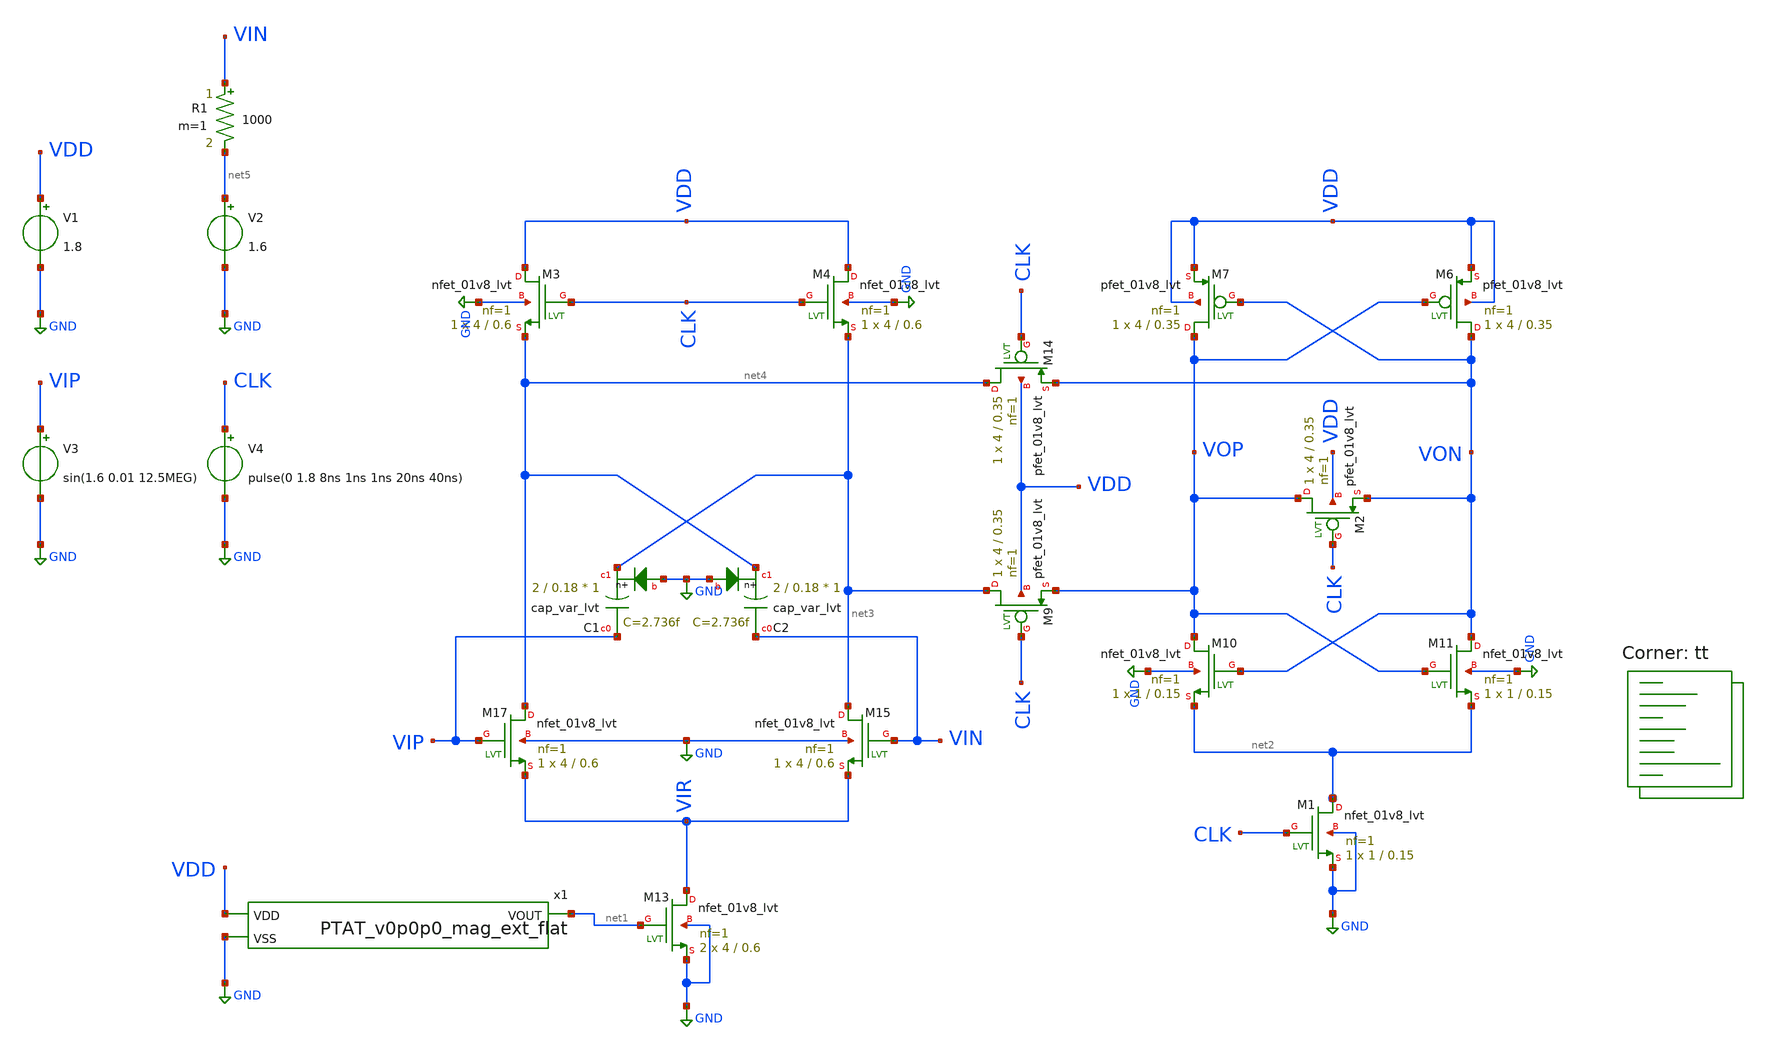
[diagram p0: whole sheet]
** sch_path: PTAT/xschem/class_AB_PTAT_ext.sch
**.subckt class_AB_PTAT_ext
XM17 net4 VIP VIR GND sky130_fd_pr__nfet_01v8_lvt L=0.6 W=4 nf=1 ad='int((nf+1)/2) * W/nf * 0.29' as='int((nf+2)/2) * W/nf * 0.29'
+ pd='2*int((nf+1)/2) * (W/nf + 0.29)' ps='2*int((nf+2)/2) * (W/nf + 0.29)' nrd='0.29 / W' nrs='0.29 / W'
+ sa=0 sb=0 sd=0 mult=1 m=1
XM15 net3 VIN VIR GND sky130_fd_pr__nfet_01v8_lvt L=0.6 W=4 nf=1 ad='int((nf+1)/2) * W/nf * 0.29' as='int((nf+2)/2) * W/nf * 0.29'
+ pd='2*int((nf+1)/2) * (W/nf + 0.29)' ps='2*int((nf+2)/2) * (W/nf + 0.29)' nrd='0.29 / W' nrs='0.29 / W'
+ sa=0 sb=0 sd=0 mult=1 m=1
XM13 VIR net1 GND GND sky130_fd_pr__nfet_01v8_lvt L=0.6 W=4 nf=1 ad='int((nf+1)/2) * W/nf * 0.29' as='int((nf+2)/2) * W/nf * 0.29'
+ pd='2*int((nf+1)/2) * (W/nf + 0.29)' ps='2*int((nf+2)/2) * (W/nf + 0.29)' nrd='0.29 / W' nrs='0.29 / W'
+ sa=0 sb=0 sd=0 mult=2 m=2
XM6 VON VOP VDD VDD sky130_fd_pr__pfet_01v8_lvt L=0.35 W=4 nf=1 ad='int((nf+1)/2) * W/nf * 0.29' as='int((nf+2)/2) * W/nf * 0.29'
+ pd='2*int((nf+1)/2) * (W/nf + 0.29)' ps='2*int((nf+2)/2) * (W/nf + 0.29)' nrd='0.29 / W' nrs='0.29 / W'
+ sa=0 sb=0 sd=0 mult=1 m=1
XM7 VOP VON VDD VDD sky130_fd_pr__pfet_01v8_lvt L=0.35 W=4 nf=1 ad='int((nf+1)/2) * W/nf * 0.29' as='int((nf+2)/2) * W/nf * 0.29'
+ pd='2*int((nf+1)/2) * (W/nf + 0.29)' ps='2*int((nf+2)/2) * (W/nf + 0.29)' nrd='0.29 / W' nrs='0.29 / W'
+ sa=0 sb=0 sd=0 mult=1 m=1
XM10 VOP VON net2 GND sky130_fd_pr__nfet_01v8_lvt L=0.15 W=1 nf=1 ad='int((nf+1)/2) * W/nf * 0.29' as='int((nf+2)/2) * W/nf * 0.29'
+ pd='2*int((nf+1)/2) * (W/nf + 0.29)' ps='2*int((nf+2)/2) * (W/nf + 0.29)' nrd='0.29 / W' nrs='0.29 / W'
+ sa=0 sb=0 sd=0 mult=1 m=1
XM11 VON VOP net2 GND sky130_fd_pr__nfet_01v8_lvt L=0.15 W=1 nf=1 ad='int((nf+1)/2) * W/nf * 0.29' as='int((nf+2)/2) * W/nf * 0.29'
+ pd='2*int((nf+1)/2) * (W/nf + 0.29)' ps='2*int((nf+2)/2) * (W/nf + 0.29)' nrd='0.29 / W' nrs='0.29 / W'
+ sa=0 sb=0 sd=0 mult=1 m=1
XM1 net2 CLK GND GND sky130_fd_pr__nfet_01v8_lvt L=0.15 W=1 nf=1 ad='int((nf+1)/2) * W/nf * 0.29' as='int((nf+2)/2) * W/nf * 0.29'
+ pd='2*int((nf+1)/2) * (W/nf + 0.29)' ps='2*int((nf+2)/2) * (W/nf + 0.29)' nrd='0.29 / W' nrs='0.29 / W'
+ sa=0 sb=0 sd=0 mult=1 m=1
XM2 VOP CLK VON VDD sky130_fd_pr__pfet_01v8_lvt L=0.35 W=4 nf=1 ad='int((nf+1)/2) * W/nf * 0.29' as='int((nf+2)/2) * W/nf * 0.29'
+ pd='2*int((nf+1)/2) * (W/nf + 0.29)' ps='2*int((nf+2)/2) * (W/nf + 0.29)' nrd='0.29 / W' nrs='0.29 / W'
+ sa=0 sb=0 sd=0 mult=1 m=1
V1 VDD GND 1.8
V3 VIP GND sin(1.6 0.01 12.5MEG)
V2 net5 GND 1.6
V4 CLK GND pulse(0 1.8 8ns 1ns 1ns 20ns 40ns)
R1 VIN net5 1000 m=1
XM9 net3 CLK VOP VDD sky130_fd_pr__pfet_01v8_lvt L=0.35 W=4 nf=1 ad='int((nf+1)/2) * W/nf * 0.29' as='int((nf+2)/2) * W/nf * 0.29'
+ pd='2*int((nf+1)/2) * (W/nf + 0.29)' ps='2*int((nf+2)/2) * (W/nf + 0.29)' nrd='0.29 / W' nrs='0.29 / W'
+ sa=0 sb=0 sd=0 mult=1 m=1
XM14 net4 CLK VON VDD sky130_fd_pr__pfet_01v8_lvt L=0.35 W=4 nf=1 ad='int((nf+1)/2) * W/nf * 0.29' as='int((nf+2)/2) * W/nf * 0.29'
+ pd='2*int((nf+1)/2) * (W/nf + 0.29)' ps='2*int((nf+2)/2) * (W/nf + 0.29)' nrd='0.29 / W' nrs='0.29 / W'
+ sa=0 sb=0 sd=0 mult=1 m=1
XM3 VDD CLK net4 GND sky130_fd_pr__nfet_01v8_lvt L=0.6 W=4 nf=1 ad='int((nf+1)/2) * W/nf * 0.29' as='int((nf+2)/2) * W/nf * 0.29'
+ pd='2*int((nf+1)/2) * (W/nf + 0.29)' ps='2*int((nf+2)/2) * (W/nf + 0.29)' nrd='0.29 / W' nrs='0.29 / W'
+ sa=0 sb=0 sd=0 mult=1 m=1
XM4 VDD CLK net3 GND sky130_fd_pr__nfet_01v8_lvt L=0.6 W=4 nf=1 ad='int((nf+1)/2) * W/nf * 0.29' as='int((nf+2)/2) * W/nf * 0.29'
+ pd='2*int((nf+1)/2) * (W/nf + 0.29)' ps='2*int((nf+2)/2) * (W/nf + 0.29)' nrd='0.29 / W' nrs='0.29 / W'
+ sa=0 sb=0 sd=0 mult=1 m=1
XC1 VIP net3 GND sky130_fd_pr__cap_var_lvt W=2 L=0.18 VM=1 m=1
XC2 VIN net4 GND sky130_fd_pr__cap_var_lvt W=2 L=0.18 VM=1 m=1
x1 VDD net1 GND PTAT_v0p0p0_mag_ext_flat
**** begin user architecture code
.lib $::SKYWATER_MODELS/sky130.lib.spice tt

.include /foss/designs/Analog_FA23_SP24/PTAT/magicext/PTAT_v0p0p0_mag_ext_flat.spice


.options savecurrents
.control

save all

tran 0.001n 120n
remzerovec
write class_AB_PTAT_ext.raw

.endc


**** end user architecture code
**.ends
.GLOBAL GND
.end
